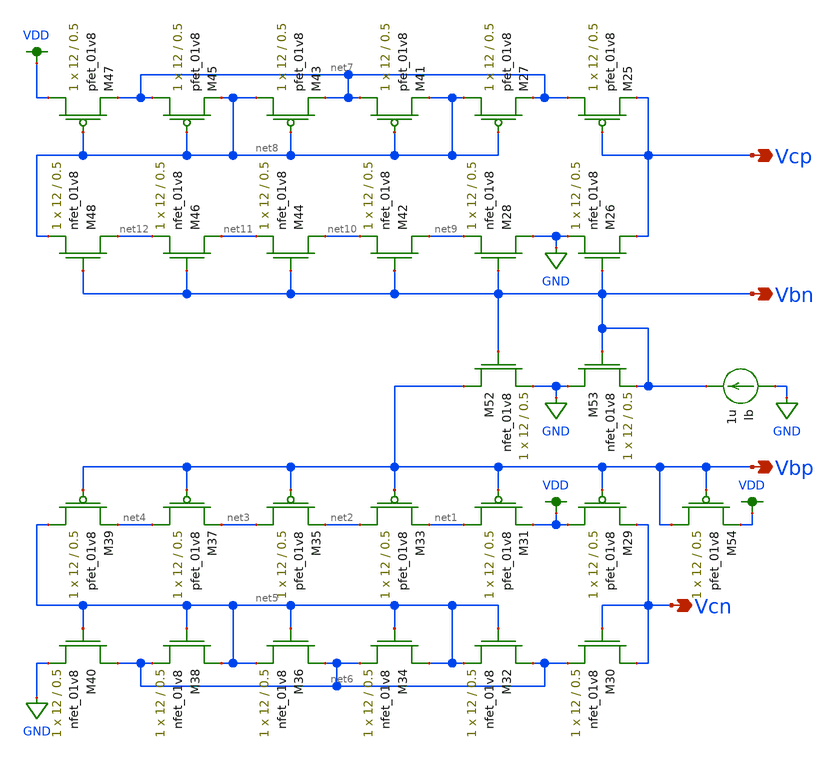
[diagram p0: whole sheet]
** sch_path: MP3/xschem/v_gen_lds_half.sch
**.subckt v_gen_lds_half Vcp Vcn Vbn Vbp
*.opin Vcp
*.opin Vcn
*.opin Vbn
*.opin Vbp
XM29 VDD Vbp Vcn VDD sky130_fd_pr__pfet_01v8 L=0.5 W=12 nf=1 ad='int((nf+1)/2) * W/nf * 0.29' as='int((nf+2)/2) * W/nf * 0.29'
+ pd='2*int((nf+1)/2) * (W/nf + 0.29)' ps='2*int((nf+2)/2) * (W/nf + 0.29)' nrd='0.29 / W' nrs='0.29 / W'
+ sa=0 sb=0 sd=0 mult=1 m=1
XM30 Vcn Vcn net6 GND sky130_fd_pr__nfet_01v8 L=0.5 W=12 nf=1 ad='int((nf+1)/2) * W/nf * 0.29' as='int((nf+2)/2) * W/nf * 0.29'
+ pd='2*int((nf+1)/2) * (W/nf + 0.29)' ps='2*int((nf+2)/2) * (W/nf + 0.29)' nrd='0.29 / W' nrs='0.29 / W'
+ sa=0 sb=0 sd=0 mult=1 m=1
XM31 net1 Vbp VDD VDD sky130_fd_pr__pfet_01v8 L=0.5 W=12 nf=1 ad='int((nf+1)/2) * W/nf * 0.29' as='int((nf+2)/2) * W/nf * 0.29'
+ pd='2*int((nf+1)/2) * (W/nf + 0.29)' ps='2*int((nf+2)/2) * (W/nf + 0.29)' nrd='0.29 / W' nrs='0.29 / W'
+ sa=0 sb=0 sd=0 mult=1 m=1
XM32 net6 net5 net5 GND sky130_fd_pr__nfet_01v8 L=0.5 W=12 nf=1 ad='int((nf+1)/2) * W/nf * 0.29' as='int((nf+2)/2) * W/nf * 0.29'
+ pd='2*int((nf+1)/2) * (W/nf + 0.29)' ps='2*int((nf+2)/2) * (W/nf + 0.29)' nrd='0.29 / W' nrs='0.29 / W'
+ sa=0 sb=0 sd=0 mult=1 m=1
XM33 net2 Vbp net1 VDD sky130_fd_pr__pfet_01v8 L=0.5 W=12 nf=1 ad='int((nf+1)/2) * W/nf * 0.29' as='int((nf+2)/2) * W/nf * 0.29'
+ pd='2*int((nf+1)/2) * (W/nf + 0.29)' ps='2*int((nf+2)/2) * (W/nf + 0.29)' nrd='0.29 / W' nrs='0.29 / W'
+ sa=0 sb=0 sd=0 mult=1 m=1
XM34 net5 net5 net6 GND sky130_fd_pr__nfet_01v8 L=0.5 W=12 nf=1 ad='int((nf+1)/2) * W/nf * 0.29' as='int((nf+2)/2) * W/nf * 0.29'
+ pd='2*int((nf+1)/2) * (W/nf + 0.29)' ps='2*int((nf+2)/2) * (W/nf + 0.29)' nrd='0.29 / W' nrs='0.29 / W'
+ sa=0 sb=0 sd=0 mult=1 m=1
XM35 net3 Vbp net2 VDD sky130_fd_pr__pfet_01v8 L=0.5 W=12 nf=1 ad='int((nf+1)/2) * W/nf * 0.29' as='int((nf+2)/2) * W/nf * 0.29'
+ pd='2*int((nf+1)/2) * (W/nf + 0.29)' ps='2*int((nf+2)/2) * (W/nf + 0.29)' nrd='0.29 / W' nrs='0.29 / W'
+ sa=0 sb=0 sd=0 mult=1 m=1
XM36 net6 net5 net5 GND sky130_fd_pr__nfet_01v8 L=0.5 W=12 nf=1 ad='int((nf+1)/2) * W/nf * 0.29' as='int((nf+2)/2) * W/nf * 0.29'
+ pd='2*int((nf+1)/2) * (W/nf + 0.29)' ps='2*int((nf+2)/2) * (W/nf + 0.29)' nrd='0.29 / W' nrs='0.29 / W'
+ sa=0 sb=0 sd=0 mult=1 m=1
XM37 net4 Vbp net3 VDD sky130_fd_pr__pfet_01v8 L=0.5 W=12 nf=1 ad='int((nf+1)/2) * W/nf * 0.29' as='int((nf+2)/2) * W/nf * 0.29'
+ pd='2*int((nf+1)/2) * (W/nf + 0.29)' ps='2*int((nf+2)/2) * (W/nf + 0.29)' nrd='0.29 / W' nrs='0.29 / W'
+ sa=0 sb=0 sd=0 mult=1 m=1
XM38 net5 net5 net6 GND sky130_fd_pr__nfet_01v8 L=0.5 W=12 nf=1 ad='int((nf+1)/2) * W/nf * 0.29' as='int((nf+2)/2) * W/nf * 0.29'
+ pd='2*int((nf+1)/2) * (W/nf + 0.29)' ps='2*int((nf+2)/2) * (W/nf + 0.29)' nrd='0.29 / W' nrs='0.29 / W'
+ sa=0 sb=0 sd=0 mult=1 m=1
XM39 net5 Vbp net4 VDD sky130_fd_pr__pfet_01v8 L=0.5 W=12 nf=1 ad='int((nf+1)/2) * W/nf * 0.29' as='int((nf+2)/2) * W/nf * 0.29'
+ pd='2*int((nf+1)/2) * (W/nf + 0.29)' ps='2*int((nf+2)/2) * (W/nf + 0.29)' nrd='0.29 / W' nrs='0.29 / W'
+ sa=0 sb=0 sd=0 mult=1 m=1
XM40 net6 net5 GND GND sky130_fd_pr__nfet_01v8 L=0.5 W=12 nf=1 ad='int((nf+1)/2) * W/nf * 0.29' as='int((nf+2)/2) * W/nf * 0.29'
+ pd='2*int((nf+1)/2) * (W/nf + 0.29)' ps='2*int((nf+2)/2) * (W/nf + 0.29)' nrd='0.29 / W' nrs='0.29 / W'
+ sa=0 sb=0 sd=0 mult=1 m=1
XM25 net7 Vcp Vcp VDD sky130_fd_pr__pfet_01v8 L=0.5 W=12 nf=1 ad='int((nf+1)/2) * W/nf * 0.29' as='int((nf+2)/2) * W/nf * 0.29'
+ pd='2*int((nf+1)/2) * (W/nf + 0.29)' ps='2*int((nf+2)/2) * (W/nf + 0.29)' nrd='0.29 / W' nrs='0.29 / W'
+ sa=0 sb=0 sd=0 mult=1 m=1
XM26 Vcp Vbn GND GND sky130_fd_pr__nfet_01v8 L=0.5 W=12 nf=1 ad='int((nf+1)/2) * W/nf * 0.29' as='int((nf+2)/2) * W/nf * 0.29'
+ pd='2*int((nf+1)/2) * (W/nf + 0.29)' ps='2*int((nf+2)/2) * (W/nf + 0.29)' nrd='0.29 / W' nrs='0.29 / W'
+ sa=0 sb=0 sd=0 mult=1 m=1
XM27 net8 net8 net7 VDD sky130_fd_pr__pfet_01v8 L=0.5 W=12 nf=1 ad='int((nf+1)/2) * W/nf * 0.29' as='int((nf+2)/2) * W/nf * 0.29'
+ pd='2*int((nf+1)/2) * (W/nf + 0.29)' ps='2*int((nf+2)/2) * (W/nf + 0.29)' nrd='0.29 / W' nrs='0.29 / W'
+ sa=0 sb=0 sd=0 mult=1 m=1
XM28 GND Vbn net9 GND sky130_fd_pr__nfet_01v8 L=0.5 W=12 nf=1 ad='int((nf+1)/2) * W/nf * 0.29' as='int((nf+2)/2) * W/nf * 0.29'
+ pd='2*int((nf+1)/2) * (W/nf + 0.29)' ps='2*int((nf+2)/2) * (W/nf + 0.29)' nrd='0.29 / W' nrs='0.29 / W'
+ sa=0 sb=0 sd=0 mult=1 m=1
XM41 net7 net8 net8 VDD sky130_fd_pr__pfet_01v8 L=0.5 W=12 nf=1 ad='int((nf+1)/2) * W/nf * 0.29' as='int((nf+2)/2) * W/nf * 0.29'
+ pd='2*int((nf+1)/2) * (W/nf + 0.29)' ps='2*int((nf+2)/2) * (W/nf + 0.29)' nrd='0.29 / W' nrs='0.29 / W'
+ sa=0 sb=0 sd=0 mult=1 m=1
XM42 net9 Vbn net10 GND sky130_fd_pr__nfet_01v8 L=0.5 W=12 nf=1 ad='int((nf+1)/2) * W/nf * 0.29' as='int((nf+2)/2) * W/nf * 0.29'
+ pd='2*int((nf+1)/2) * (W/nf + 0.29)' ps='2*int((nf+2)/2) * (W/nf + 0.29)' nrd='0.29 / W' nrs='0.29 / W'
+ sa=0 sb=0 sd=0 mult=1 m=1
XM43 net8 net8 net7 VDD sky130_fd_pr__pfet_01v8 L=0.5 W=12 nf=1 ad='int((nf+1)/2) * W/nf * 0.29' as='int((nf+2)/2) * W/nf * 0.29'
+ pd='2*int((nf+1)/2) * (W/nf + 0.29)' ps='2*int((nf+2)/2) * (W/nf + 0.29)' nrd='0.29 / W' nrs='0.29 / W'
+ sa=0 sb=0 sd=0 mult=1 m=1
XM44 net10 Vbn net11 GND sky130_fd_pr__nfet_01v8 L=0.5 W=12 nf=1 ad='int((nf+1)/2) * W/nf * 0.29' as='int((nf+2)/2) * W/nf * 0.29'
+ pd='2*int((nf+1)/2) * (W/nf + 0.29)' ps='2*int((nf+2)/2) * (W/nf + 0.29)' nrd='0.29 / W' nrs='0.29 / W'
+ sa=0 sb=0 sd=0 mult=1 m=1
XM45 net7 net8 net8 VDD sky130_fd_pr__pfet_01v8 L=0.5 W=12 nf=1 ad='int((nf+1)/2) * W/nf * 0.29' as='int((nf+2)/2) * W/nf * 0.29'
+ pd='2*int((nf+1)/2) * (W/nf + 0.29)' ps='2*int((nf+2)/2) * (W/nf + 0.29)' nrd='0.29 / W' nrs='0.29 / W'
+ sa=0 sb=0 sd=0 mult=1 m=1
XM46 net11 Vbn net12 GND sky130_fd_pr__nfet_01v8 L=0.5 W=12 nf=1 ad='int((nf+1)/2) * W/nf * 0.29' as='int((nf+2)/2) * W/nf * 0.29'
+ pd='2*int((nf+1)/2) * (W/nf + 0.29)' ps='2*int((nf+2)/2) * (W/nf + 0.29)' nrd='0.29 / W' nrs='0.29 / W'
+ sa=0 sb=0 sd=0 mult=1 m=1
XM47 VDD net8 net7 VDD sky130_fd_pr__pfet_01v8 L=0.5 W=12 nf=1 ad='int((nf+1)/2) * W/nf * 0.29' as='int((nf+2)/2) * W/nf * 0.29'
+ pd='2*int((nf+1)/2) * (W/nf + 0.29)' ps='2*int((nf+2)/2) * (W/nf + 0.29)' nrd='0.29 / W' nrs='0.29 / W'
+ sa=0 sb=0 sd=0 mult=1 m=1
XM48 net12 Vbn net8 GND sky130_fd_pr__nfet_01v8 L=0.5 W=12 nf=1 ad='int((nf+1)/2) * W/nf * 0.29' as='int((nf+2)/2) * W/nf * 0.29'
+ pd='2*int((nf+1)/2) * (W/nf + 0.29)' ps='2*int((nf+2)/2) * (W/nf + 0.29)' nrd='0.29 / W' nrs='0.29 / W'
+ sa=0 sb=0 sd=0 mult=1 m=1
XM52 Vbp Vbn GND GND sky130_fd_pr__nfet_01v8 L=0.5 W=12 nf=1 ad='int((nf+1)/2) * W/nf * 0.29' as='int((nf+2)/2) * W/nf * 0.29'
+ pd='2*int((nf+1)/2) * (W/nf + 0.29)' ps='2*int((nf+2)/2) * (W/nf + 0.29)' nrd='0.29 / W' nrs='0.29 / W'
+ sa=0 sb=0 sd=0 mult=1 m=1
XM53 GND Vbn Vbn GND sky130_fd_pr__nfet_01v8 L=0.5 W=12 nf=1 ad='int((nf+1)/2) * W/nf * 0.29' as='int((nf+2)/2) * W/nf * 0.29'
+ pd='2*int((nf+1)/2) * (W/nf + 0.29)' ps='2*int((nf+2)/2) * (W/nf + 0.29)' nrd='0.29 / W' nrs='0.29 / W'
+ sa=0 sb=0 sd=0 mult=1 m=1
XM54 Vbp Vbp VDD VDD sky130_fd_pr__pfet_01v8 L=0.5 W=12 nf=1 ad='int((nf+1)/2) * W/nf * 0.29' as='int((nf+2)/2) * W/nf * 0.29'
+ pd='2*int((nf+1)/2) * (W/nf + 0.29)' ps='2*int((nf+2)/2) * (W/nf + 0.29)' nrd='0.29 / W' nrs='0.29 / W'
+ sa=0 sb=0 sd=0 mult=1 m=1
Ib GND Vbn 1u
**.ends
.GLOBAL GND
.GLOBAL VDD
.end
